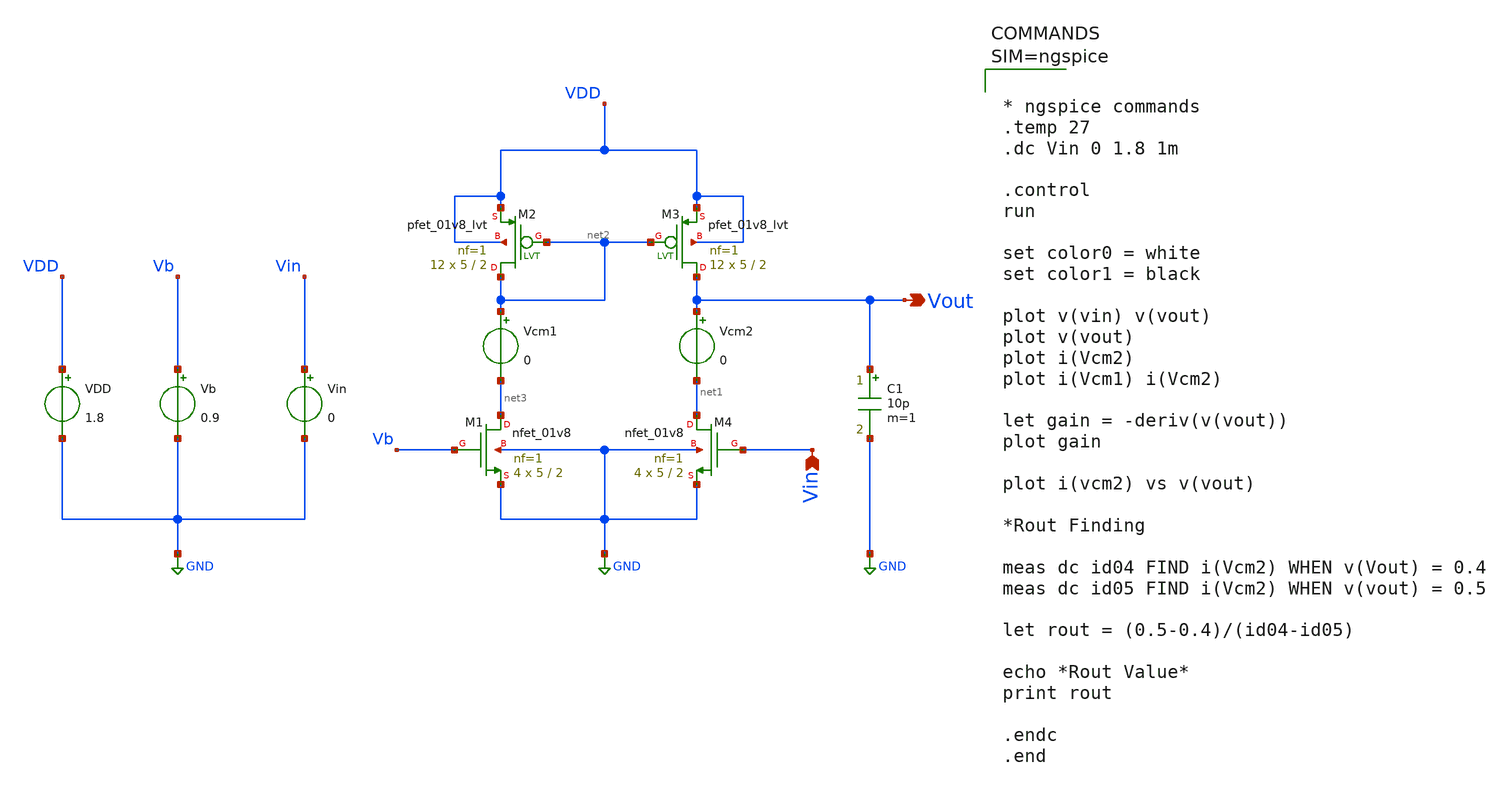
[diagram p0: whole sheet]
** sch_path: Common_Source_PMOS_Current_Source_Load_ckts/CS_Amp_PMOS_Current_Source_Load_ckt.sch
**.subckt CS_Amp_PMOS_Current_Source_Load_ckt Vout Vin
*.opin Vout
*.ipin Vin
XM1 net3 Vb GND GND sky130_fd_pr__nfet_01v8 L=2 W=5 nf=1 ad='int((1 + 1)/2) * 5 / 1 * 0.29' as='int((1 + 2)/2) * 5 / 1 * 0.29'
+ pd='2*int((1 + 1)/2) * (5 / 1 + 0.29)' ps='2*int((1 + 2)/2) * (5 / 1 + 0.29)' nrd='0.29 / 5 ' nrs='0.29 / 5 '
+ sa=0 sb=0 sd=0 mult=4 m=4
XM2 net2 net2 VDD VDD sky130_fd_pr__pfet_01v8_lvt L=2 W=5 nf=1 ad='int((1 + 1)/2) * 5 / 1 * 0.29' as='int((1 + 2)/2) * 5 / 1 * 0.29'
+ pd='2*int((1 + 1)/2) * (5 / 1 + 0.29)' ps='2*int((1 + 2)/2) * (5 / 1 + 0.29)' nrd='0.29 / 5 ' nrs='0.29 / 5 '
+ sa=0 sb=0 sd=0 mult=12 m=12
XM3 Vout net2 VDD VDD sky130_fd_pr__pfet_01v8_lvt L=2 W=5 nf=1 ad='int((1 + 1)/2) * 5 / 1 * 0.29' as='int((1 + 2)/2) * 5 / 1 * 0.29'
+ pd='2*int((1 + 1)/2) * (5 / 1 + 0.29)' ps='2*int((1 + 2)/2) * (5 / 1 + 0.29)' nrd='0.29 / 5 ' nrs='0.29 / 5 '
+ sa=0 sb=0 sd=0 mult=12 m=12
XM4 net1 Vin GND GND sky130_fd_pr__nfet_01v8 L=2 W=5 nf=1 ad='int((1 + 1)/2) * 5 / 1 * 0.29' as='int((1 + 2)/2) * 5 / 1 * 0.29'
+ pd='2*int((1 + 1)/2) * (5 / 1 + 0.29)' ps='2*int((1 + 2)/2) * (5 / 1 + 0.29)' nrd='0.29 / 5 ' nrs='0.29 / 5 '
+ sa=0 sb=0 sd=0 mult=4 m=4
Vb Vb GND 0.9
Vin Vin GND 0
VDD VDD GND 1.8
Vcm1 net2 net3 0
Vcm2 Vout net1 0
C1 Vout GND 10p m=1
**** begin user architecture code



* ngspice commands
.temp 27
.dc Vin 0 1.8 1m

.control
run

set color0 = white
set color1 = black

plot v(vin) v(vout)
plot v(vout)
plot i(Vcm2)
plot i(Vcm1) i(Vcm2)

let gain = -deriv(v(vout))
plot gain

plot i(vcm2) vs v(vout)

*Rout Finding

meas dc id04 FIND i(Vcm2) WHEN v(Vout) = 0.4
meas dc id05 FIND i(Vcm2) WHEN v(vout) = 0.5

let rout = (0.5-0.4)/(id04-id05)

echo *Rout Value*
print rout

.endc
.end






** opencircuitdesign pdks install
.lib $::SKYWATER_MODELS/sky130.lib.spice tt

**** end user architecture code
**.ends
.GLOBAL GND
.end
